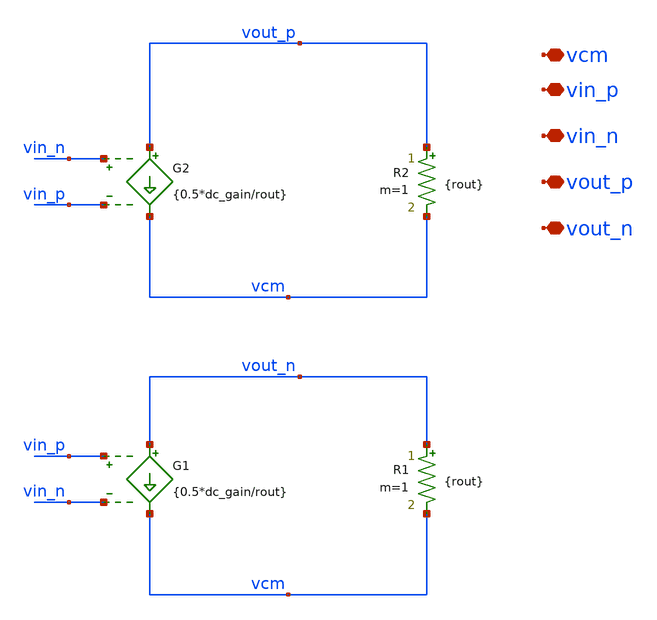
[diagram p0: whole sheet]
** sch_path: xschem/ota_bhv/ota_bhv.sch
**.subckt ota_bhv vcm vin_p vin_n vout_p vout_n
*.iopin vcm
*.iopin vin_p
*.iopin vin_n
*.iopin vout_p
*.iopin vout_n
G1 vout_n vcm vin_p vin_n {0.5*dc_gain/rout}
R1 vout_n vcm {rout} m=1
G2 vout_p vcm vin_n vin_p {0.5*dc_gain/rout}
R2 vout_p vcm {rout} m=1
**.ends
.end
